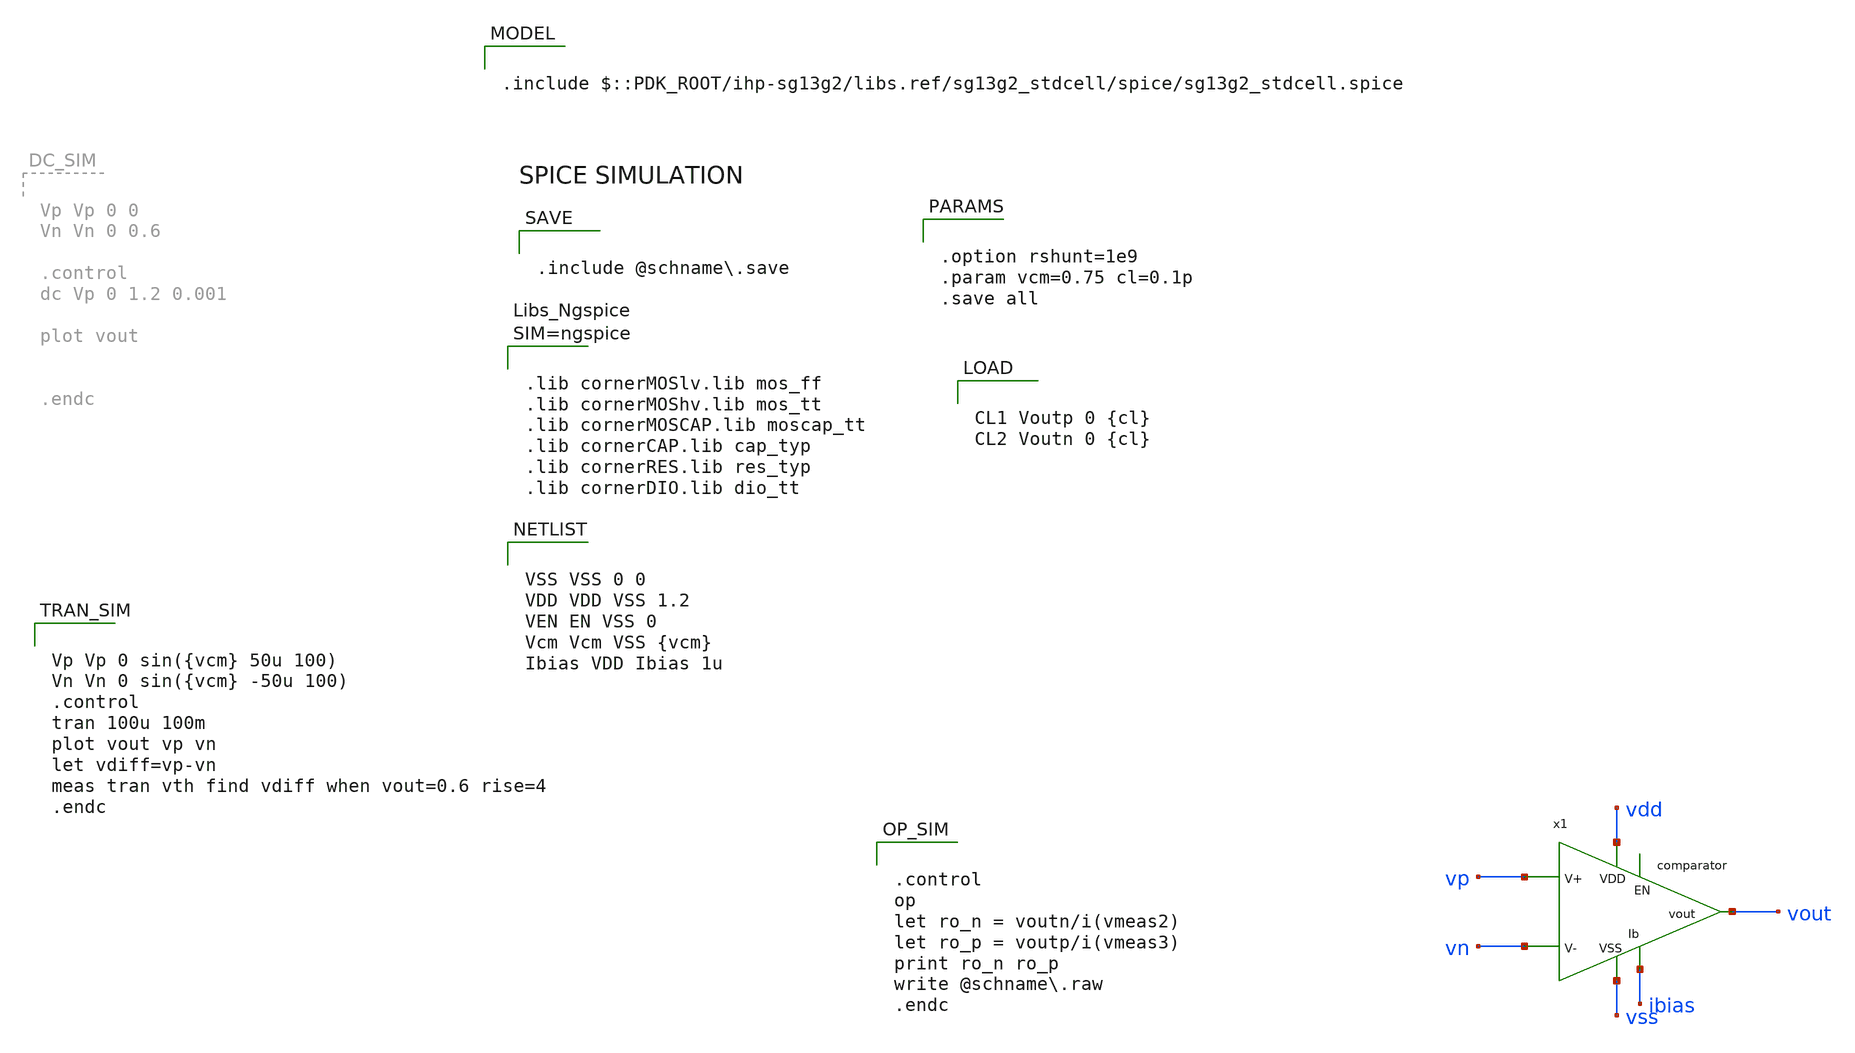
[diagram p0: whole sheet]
** sch_path: schematic/xschem/comparator/comparator_tb.sch

.include $::PDK_ROOT/ihp-sg13g2/libs.ref/sg13g2_stdcell/spice/sg13g2_stdcell.spice


**.subckt comparator_tb
x1 vdd vout vp vn ibias vss comparator
**** begin user architecture code


VSS VSS 0 0
VDD VDD VSS 1.2
VEN EN VSS 0
Vcm Vcm VSS {vcm}
Ibias VDD Ibias 1u



.control
op
let ro_n = voutn/i(vmeas2)
let ro_p = voutp/i(vmeas3)
print ro_n ro_p
write @schname.raw
.endc




.lib cornerMOSlv.lib mos_ff
.lib cornerMOShv.lib mos_tt
.lib cornerMOSCAP.lib moscap_tt
.lib cornerCAP.lib cap_typ
.lib cornerRES.lib res_typ
.lib cornerDIO.lib dio_tt





.option rshunt=1e9
.param vcm=0.75 cl=0.1p
.save all




CL1 Voutp 0 {cl}
CL2 Voutn 0 {cl}



.include @schname.save



Vp Vp 0 sin({vcm} 50u 100)
Vn Vn 0 sin({vcm} -50u 100)
.control
tran 100u 100m
plot vout vp vn
let vdiff=vp-vn
meas tran vth find vdiff when vout=0.6 rise=4
.endc


**** end user architecture code
**.ends

* expanding   symbol:  comparator/comparator.sym # of pins=6
** sym_path: schematic/xschem/comparator/comparator.sym
** sch_path: schematic/xschem/comparator/comparator.sch
.subckt comparator vdd vout v- v+ iout vss
*.iopin vdd
*.iopin vss
*.iopin v-
*.iopin v+
*.iopin iout
*.iopin vout
XM6 votap v+ net1 vss sg13_lv_nmos w=0.26u l=3u ng=1 m=2 mm_ok=1
XM8 vdd votap votap vdd sg13_lv_pmos w=0.35u l=1u ng=1 m=2 mm_ok=1
XM9 votan v- net1 vss sg13_lv_nmos w=0.26u l=3u ng=1 m=2 mm_ok=1
XM10 vdd votan votan vdd sg13_lv_pmos w=0.35u l=1u ng=1 m=2 mm_ok=1
XM11 net1 iout vss vss sg13_lv_nmos w=2u l=5u ng=1 m=2 mm_ok=1
x1 vdd votan vom vop vss vss decision_circuit
x2 vdd votap vop vom vss vss decision_circuit
x3 net3 net2 VDD VSS sg13g2_inv_16
x4 vdd iout vop vom net2 vss final_stage_ota
x5 vout net3 VDD VSS sg13g2_inv_16
.ends


* expanding   symbol:
*+  /foss/designs/ic_design/chipaloza/schema/decision_circuit/decision_circuit.sym # of pins=6
** sym_path: schematic/xschem/decision_circuit/decision_circuit.sym
** sch_path: schematic/xschem/decision_circuit/decision_circuit.sch
.subckt decision_circuit vdd vota vout vota_n vss shift
*.iopin vota
*.iopin shift
*.iopin vota_n
*.iopin vdd
*.iopin vss
*.iopin vout
XM1 vout vota vdd vdd sg13_lv_pmos w=0.7u l=1u ng=1 m=1 mm_ok=1
XM2 vout vout shift vss sg13_lv_nmos w=0.26u l=10u ng=1 m=2 mm_ok=1
XM3 vout vota_n shift vss sg13_lv_nmos w=0.26u l=10u ng=1 m=2 mm_ok=1
XM4 vss vss vout vss sg13_lv_nmos w=0.26u l=0.5u ng=1 m=4 mm_ok=1
XM5 vdd vdd vout vdd sg13_lv_pmos w=0.35u l=0.5u ng=1 m=2 mm_ok=1
.ends


* expanding   symbol:  /foss/designs/ic_design/chipaloza/schema/final_stage_ota/final_stage_ota.sym
*+ # of pins=6
** sym_path: schematic/xschem/final_stage_ota/final_stage_ota.sym
** sch_path: schematic/xschem/final_stage_ota/final_stage_ota.sch
.subckt final_stage_ota vdd iout vop vom vout vss
*.iopin vdd
*.iopin vom
*.iopin vop
*.iopin vss
*.iopin vout
*.iopin iout
XM1 vdd ibp vt vdd sg13_lv_pmos w=1u l=3u ng=1 m=2 mm_ok=1
XM2 net1 net1 vss vss sg13_lv_nmos w=0.15u l=3u ng=1 m=2 mm_ok=1
XM3 vt vom net1 vdd sg13_lv_pmos w=3.12u l=1u ng=1 m=2 mm_ok=1
XM4 vout net1 vss vss sg13_lv_nmos w=0.15u l=3u ng=1 m=2 mm_ok=1
XM5 vt vop vout vdd sg13_lv_pmos w=3.12u l=1u ng=1 m=2 mm_ok=1
XM6 ibp iout vss vss sg13_lv_nmos w=2u l=5u ng=1 m=1 mm_ok=1
XM7 vdd ibp ibp vdd sg13_lv_pmos w=1u l=3u ng=1 m=1 mm_ok=1
.ends

.end
